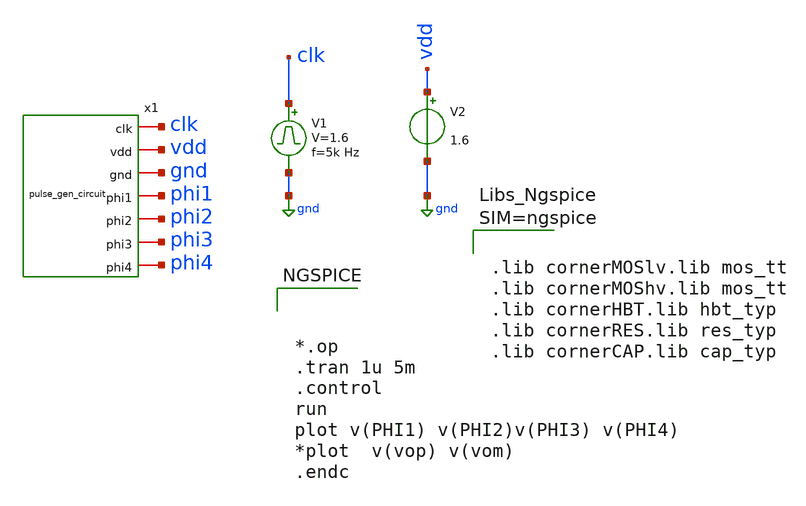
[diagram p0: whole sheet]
** sch_path: Clock_gen_using_transistor_hv/test.sch
**.subckt test
V2 vdd gnd 1.6
V1 clk gnd pulse 0 1.6 '0.495/ 5k ' '0.01/5k ' '0.01/5k ' '0.49/5k ' '1/5k '
x1 clk vdd gnd phi1 phi2 phi3 phi4 pulse_gen_circuit
**** begin user architecture code



*.op
.tran 1u 5m
.control
run
plot v(PHI1) v(PHI2)v(PHI3) v(PHI4)
*plot  v(vop) v(vom)
.endc





.lib cornerMOSlv.lib mos_tt
.lib cornerMOShv.lib mos_tt
.lib cornerHBT.lib hbt_typ
.lib cornerRES.lib res_typ
.lib cornerCAP.lib cap_typ



**** end user architecture code
**.ends

* expanding   symbol:
*+  /home/designer/shared/uni_cass/final_Design_file/Clock_gen_using_transistor_hv/pulse_gen_circuit.sym # of pins=7
** sym_path: /home/designer/shared/uni_cass/final_Design_file/Clock_gen_using_transistor_hv/pulse_gen_circuit.sym
** sch_path: /home/designer/shared/uni_cass/final_Design_file/Clock_gen_using_transistor_hv/pulse_gen_circuit.sch
.subckt pulse_gen_circuit clk vdd gnd phi1 phi2 phi3 phi4
*.iopin vdd
*.iopin gnd
*.iopin phi1
*.iopin phi2
*.iopin phi3
*.iopin phi4
*.iopin clk
x1 vdd x out1 gnd phi4 and
x2 vdd y net1 gnd phi3 and
x4 vdd phi2 clk gnd x nor
x6 vdd clk_bar phi1 gnd y nor
x7 clk clk_bar vdd gnd inverter
x8 phi1 out1 vdd gnd buffer
x9 phi2 net1 vdd gnd buffer
x3 x phi1 vdd gnd buffer
x5 y phi2 vdd gnd buffer
.ends


* expanding   symbol:
*+  /home/designer/shared/uni_cass/final_Design_file/Clock_gen_using_transistor_hv/and.sym # of pins=5
** sym_path: /home/designer/shared/uni_cass/final_Design_file/Clock_gen_using_transistor_hv/and.sym
** sch_path: /home/designer/shared/uni_cass/final_Design_file/Clock_gen_using_transistor_hv/and.sch
.subckt and vdd B A gnd out
*.iopin vdd
*.iopin B
*.iopin A
*.iopin gnd
*.iopin out
XM3 net1 A vdd vdd sg13_hv_pmos w=0.3u l=0.45u ng=1 m=1 mm_ok=1
XM1 net2 B gnd gnd sg13_hv_nmos w=0.3u l=0.45u ng=1 m=1 mm_ok=1
XM2 net1 A net2 net2 sg13_hv_nmos w=0.3u l=0.45u ng=1 m=1 mm_ok=1
XM4 net1 B vdd vdd sg13_hv_pmos w=0.3u l=0.45u ng=1 m=1 mm_ok=1
XM5 out net1 vdd vdd sg13_hv_pmos w=0.3u l=0.45u ng=1 m=1 mm_ok=1
XM6 out net1 gnd gnd sg13_hv_nmos w=0.3u l=0.45u ng=1 m=1 mm_ok=1
.ends


* expanding   symbol:
*+  /home/designer/shared/uni_cass/final_Design_file/Clock_gen_using_transistor_hv/nor.sym # of pins=5
** sym_path: /home/designer/shared/uni_cass/final_Design_file/Clock_gen_using_transistor_hv/nor.sym
** sch_path: /home/designer/shared/uni_cass/final_Design_file/Clock_gen_using_transistor_hv/nor.sch
.subckt nor vdd B A gnd out
*.iopin vdd
*.iopin B
*.iopin A
*.iopin gnd
*.iopin out
XM3 net1 A vdd vdd sg13_hv_pmos w=0.3u l=0.45u ng=1 m=1 mm_ok=1
XM1 out B gnd gnd sg13_hv_nmos w=0.3u l=0.45u ng=1 m=1 mm_ok=1
XM2 out A gnd gnd sg13_hv_nmos w=0.3u l=0.45u ng=1 m=1 mm_ok=1
XM4 out B net1 net1 sg13_hv_pmos w=0.3u l=0.45u ng=1 m=1 mm_ok=1
.ends


* expanding   symbol:
*+  /home/designer/shared/uni_cass/final_Design_file/Clock_gen_using_transistor_hv/inverter.sym # of pins=4
** sym_path: /home/designer/shared/uni_cass/final_Design_file/Clock_gen_using_transistor_hv/inverter.sym
** sch_path: /home/designer/shared/uni_cass/final_Design_file/Clock_gen_using_transistor_hv/inverter.sch
.subckt inverter in out vdd gnd
*.iopin in
*.iopin vdd
*.iopin out
*.iopin gnd
XM3 out in vdd vdd sg13_hv_pmos w=2u l=2u ng=1 m=1 mm_ok=1
XM1 out in gnd gnd sg13_hv_nmos w=1u l=1u ng=1 m=1 mm_ok=1
.ends


* expanding   symbol:
*+  /home/designer/shared/uni_cass/final_Design_file/Clock_gen_using_transistor_hv/buffer.sym # of pins=4
** sym_path: /home/designer/shared/uni_cass/final_Design_file/Clock_gen_using_transistor_hv/buffer.sym
** sch_path: /home/designer/shared/uni_cass/final_Design_file/Clock_gen_using_transistor_hv/buffer.sch
.subckt buffer in out vdd gnd
*.iopin in
*.iopin out
*.iopin vdd
*.iopin gnd
x1 in net1 vdd gnd inverter
x2 net1 out vdd gnd inverter
.ends

.GLOBAL gnd
.end
